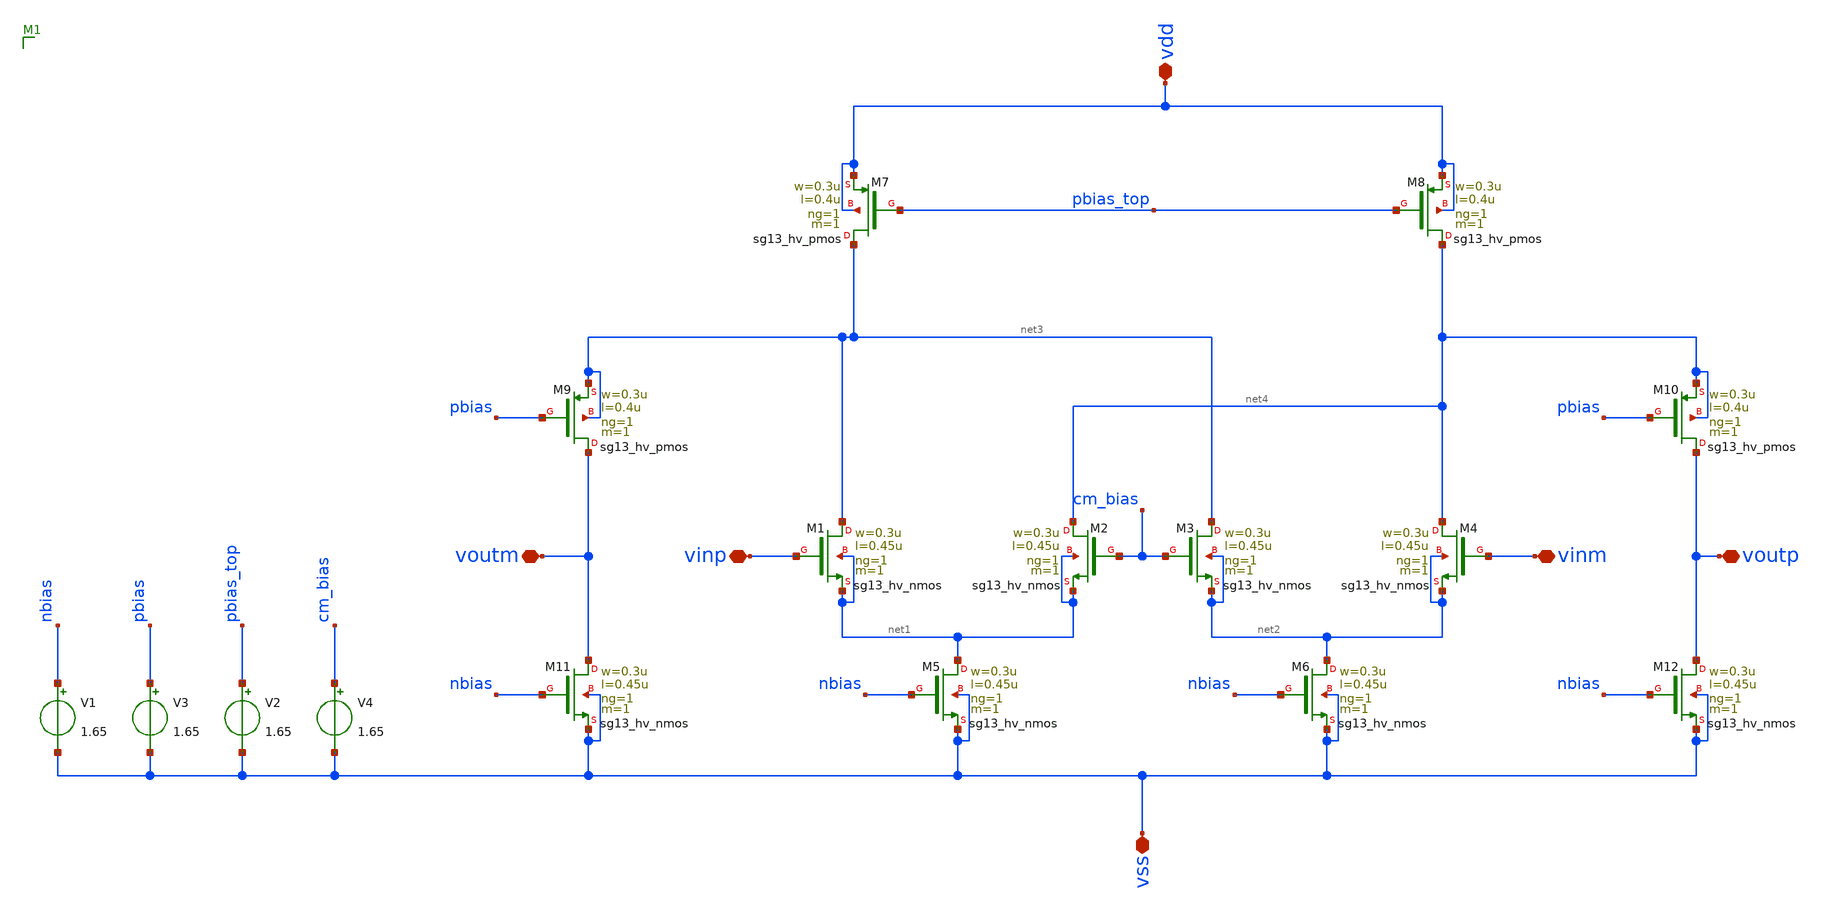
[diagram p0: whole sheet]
** sch_path: schematic/aux_amp.sch
**.subckt aux_amp vss voutm vinp vdd voutp vinm
*.iopin vss
*.iopin voutm
*.iopin vinp
*.iopin vdd
*.iopin voutp
*.iopin vinm
XM1 net3 vinp net1 net1 sg13_hv_nmos w=0.3u l=0.45u ng=1 m=1 mm_ok=1
XM2 net4 cm_bias net1 net1 sg13_hv_nmos w=0.3u l=0.45u ng=1 m=1 mm_ok=1
XM5 net1 nbias vss vss sg13_hv_nmos w=0.3u l=0.45u ng=1 m=1 mm_ok=1
XM3 net3 cm_bias net2 net2 sg13_hv_nmos w=0.3u l=0.45u ng=1 m=1 mm_ok=1
XM4 net4 vinm net2 net2 sg13_hv_nmos w=0.3u l=0.45u ng=1 m=1 mm_ok=1
XM6 net2 nbias vss vss sg13_hv_nmos w=0.3u l=0.45u ng=1 m=1 mm_ok=1
XM11 voutm nbias vss vss sg13_hv_nmos w=0.3u l=0.45u ng=1 m=1 mm_ok=1
XM12 voutp nbias vss vss sg13_hv_nmos w=0.3u l=0.45u ng=1 m=1 mm_ok=1
V2 pbias_top vss 1.65
V3 pbias vss 1.65
V4 cm_bias vss 1.65
V1 nbias vss 1.65
XM9 voutm pbias net3 net3 sg13_hv_pmos w=0.3u l=0.4u ng=1 m=1 mm_ok=1
XM7 net3 pbias_top vdd vdd sg13_hv_pmos w=0.3u l=0.4u ng=1 m=1 mm_ok=1
XM8 net4 pbias_top vdd vdd sg13_hv_pmos w=0.3u l=0.4u ng=1 m=1 mm_ok=1
XM10 voutp pbias net4 net4 sg13_hv_pmos w=0.3u l=0.4u ng=1 m=1 mm_ok=1
**.ends
.end
